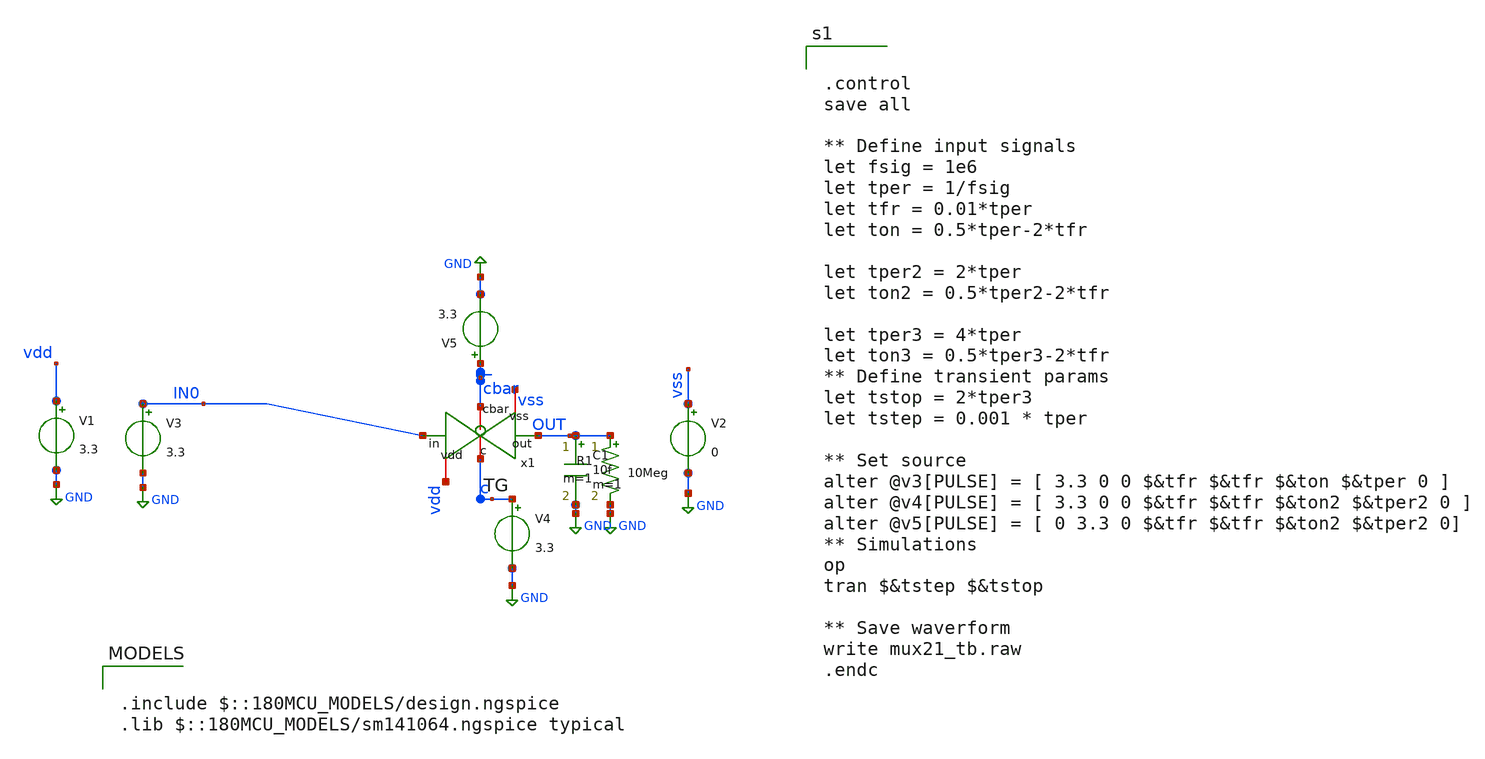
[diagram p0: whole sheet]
** sch_path: schematics/PC/TG/TG_tb.sch
**.subckt TG_tb
V2 vss GND 0
V1 vdd GND 3.3
V3 IN0 GND 3.3
V5 cbar GND 3.3
C1 OUT GND 10f m=1
V4 c GND 3.3
R1 OUT GND 10Meg m=1
x1 IN0 vss vdd c cbar OUT TG
**** begin user architecture code

.include $::180MCU_MODELS/design.ngspice
.lib $::180MCU_MODELS/sm141064.ngspice typical



.control
save all

** Define input signals
let fsig = 1e6
let tper = 1/fsig
let tfr = 0.01*tper
let ton = 0.5*tper-2*tfr

let tper2 = 2*tper
let ton2 = 0.5*tper2-2*tfr

let tper3 = 4*tper
let ton3 = 0.5*tper3-2*tfr
** Define transient params
let tstop = 2*tper3
let tstep = 0.001 * tper

** Set source
alter @v3[PULSE] = [ 3.3 0 0 $&tfr $&tfr $&ton $&tper 0 ]
alter @v4[PULSE] = [ 3.3 0 0 $&tfr $&tfr $&ton2 $&tper2 0 ]
alter @v5[PULSE] = [ 0 3.3 0 $&tfr $&tfr $&ton2 $&tper2 0]
** Simulations
op
tran $&tstep $&tstop

** Save waverform
write mux21_tb.raw
.endc



**** end user architecture code
**.ends

* expanding   symbol:  CAD2/TG.sym # of pins=6
** sym_path: schematics/PC/TG/TG.sym
** sch_path: schematics/PC/TG/TG.sch
.subckt TG in vss vdd c cbar out
*.ipin in
*.opin out
*.iopin vss
*.iopin vdd
*.iopin c
*.iopin cbar
XM1 out cbar in vdd pfet_03v3 L=0.28u W=2u nf=1 ad='int((nf+1)/2) * W/nf * 0.18u' as='int((nf+2)/2) * W/nf * 0.18u'
+ pd='2*int((nf+1)/2) * (W/nf + 0.18u)' ps='2*int((nf+2)/2) * (W/nf + 0.18u)' nrd='0.18u / W' nrs='0.18u / W'
+ sa=0 sb=0 sd=0 m=1
XM2 in c out vss nfet_03v3 L=0.28u W=1u nf=1 ad='int((nf+1)/2) * W/nf * 0.18u' as='int((nf+2)/2) * W/nf * 0.18u'
+ pd='2*int((nf+1)/2) * (W/nf + 0.18u)' ps='2*int((nf+2)/2) * (W/nf + 0.18u)' nrd='0.18u / W' nrs='0.18u / W'
+ sa=0 sb=0 sd=0 m=1
.ends

.GLOBAL GND
.end
